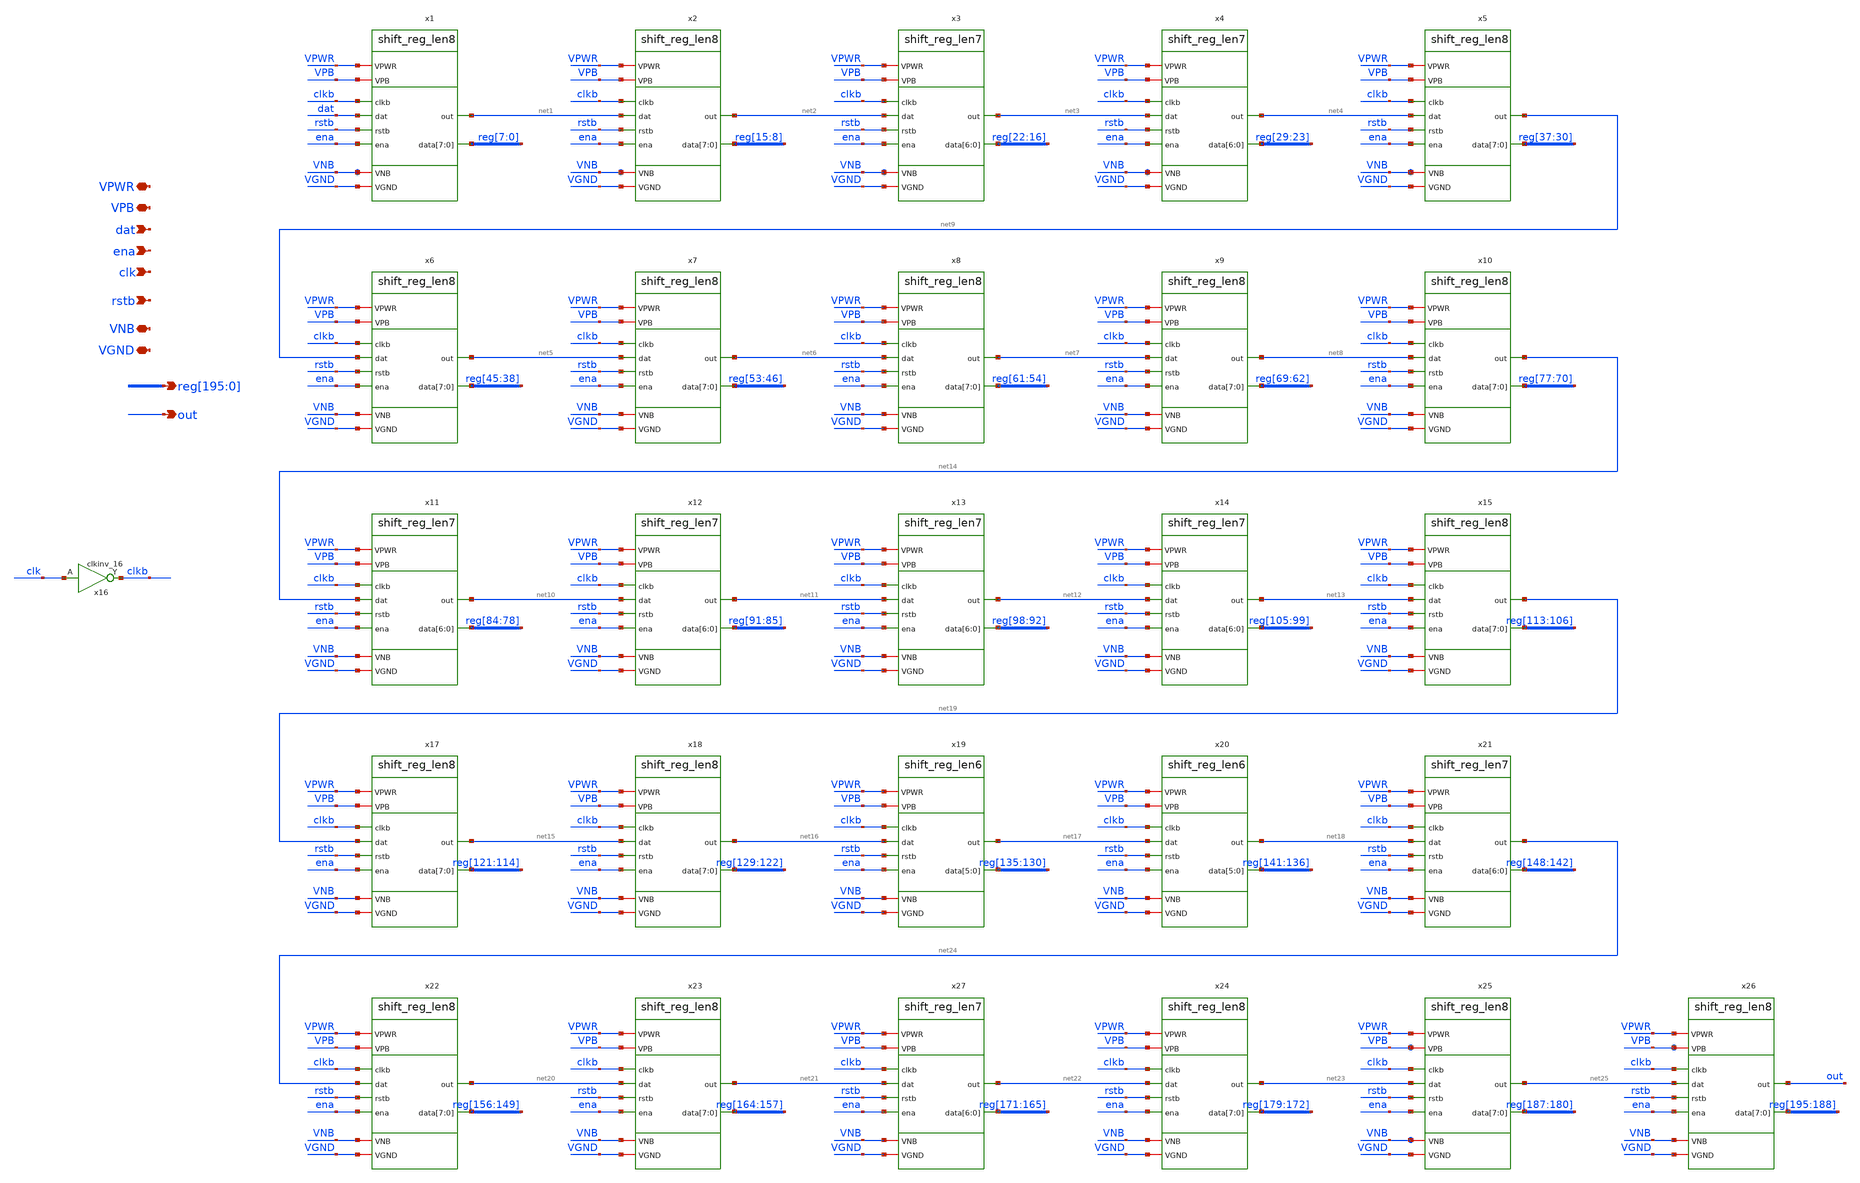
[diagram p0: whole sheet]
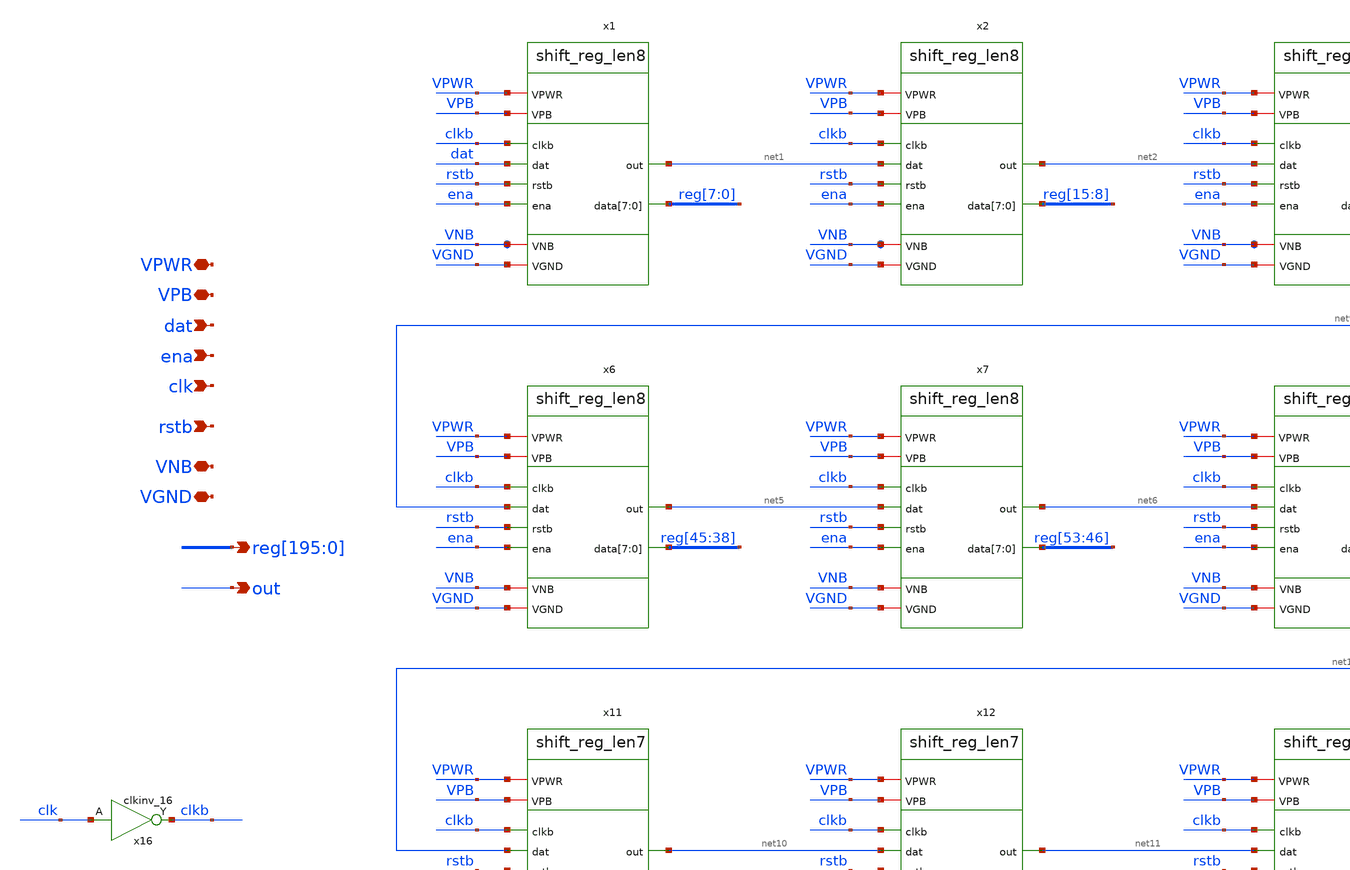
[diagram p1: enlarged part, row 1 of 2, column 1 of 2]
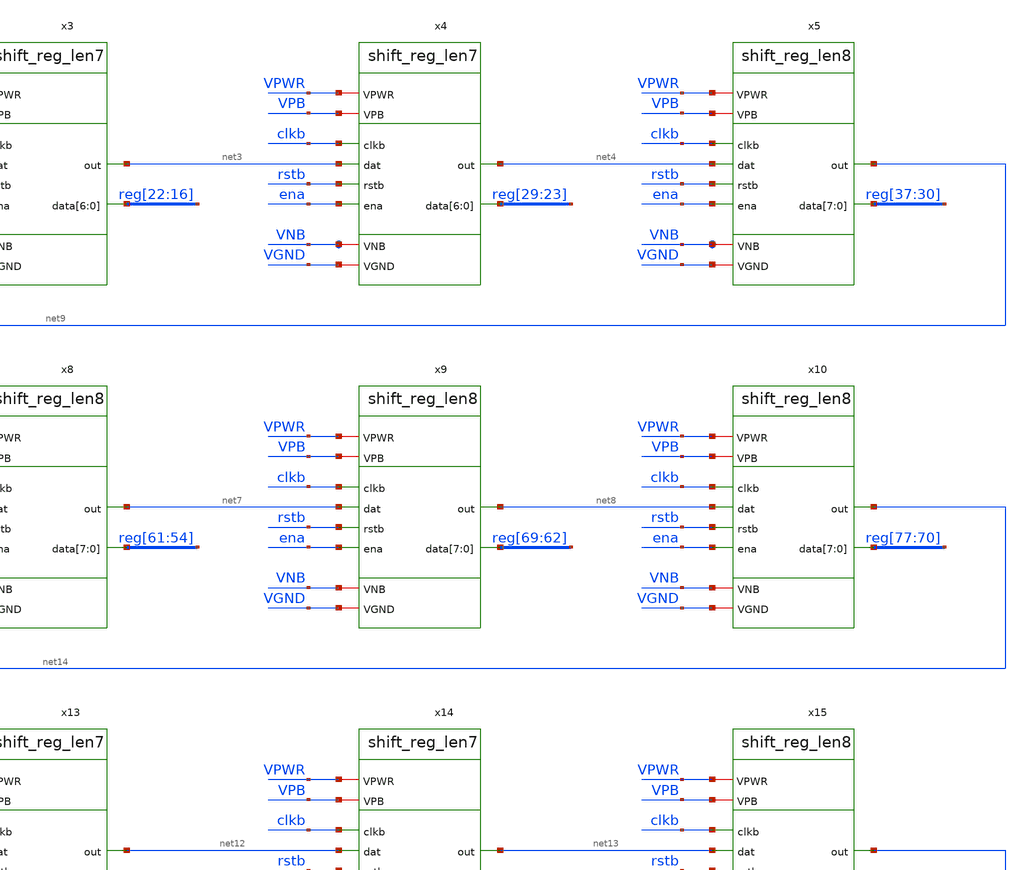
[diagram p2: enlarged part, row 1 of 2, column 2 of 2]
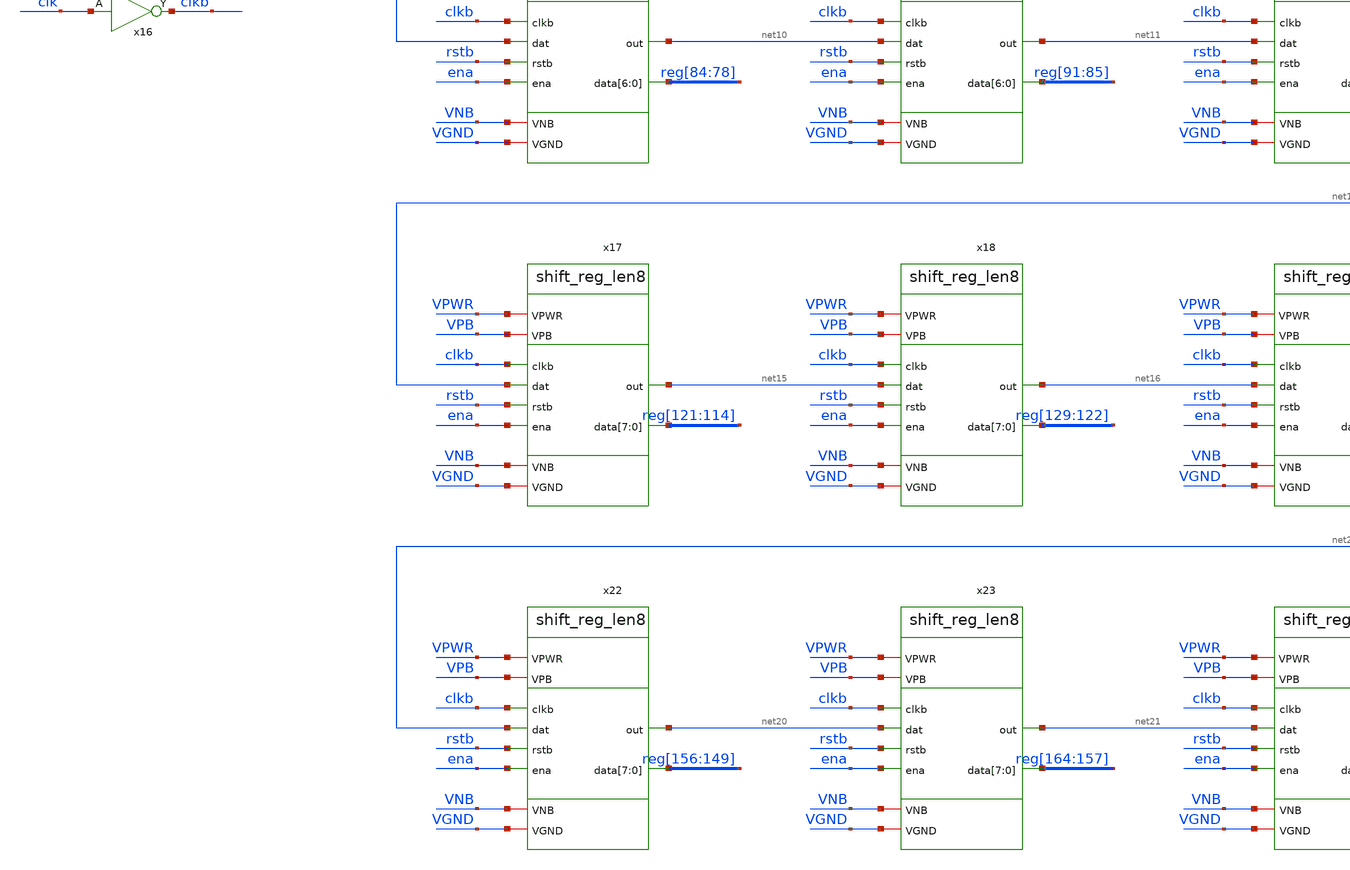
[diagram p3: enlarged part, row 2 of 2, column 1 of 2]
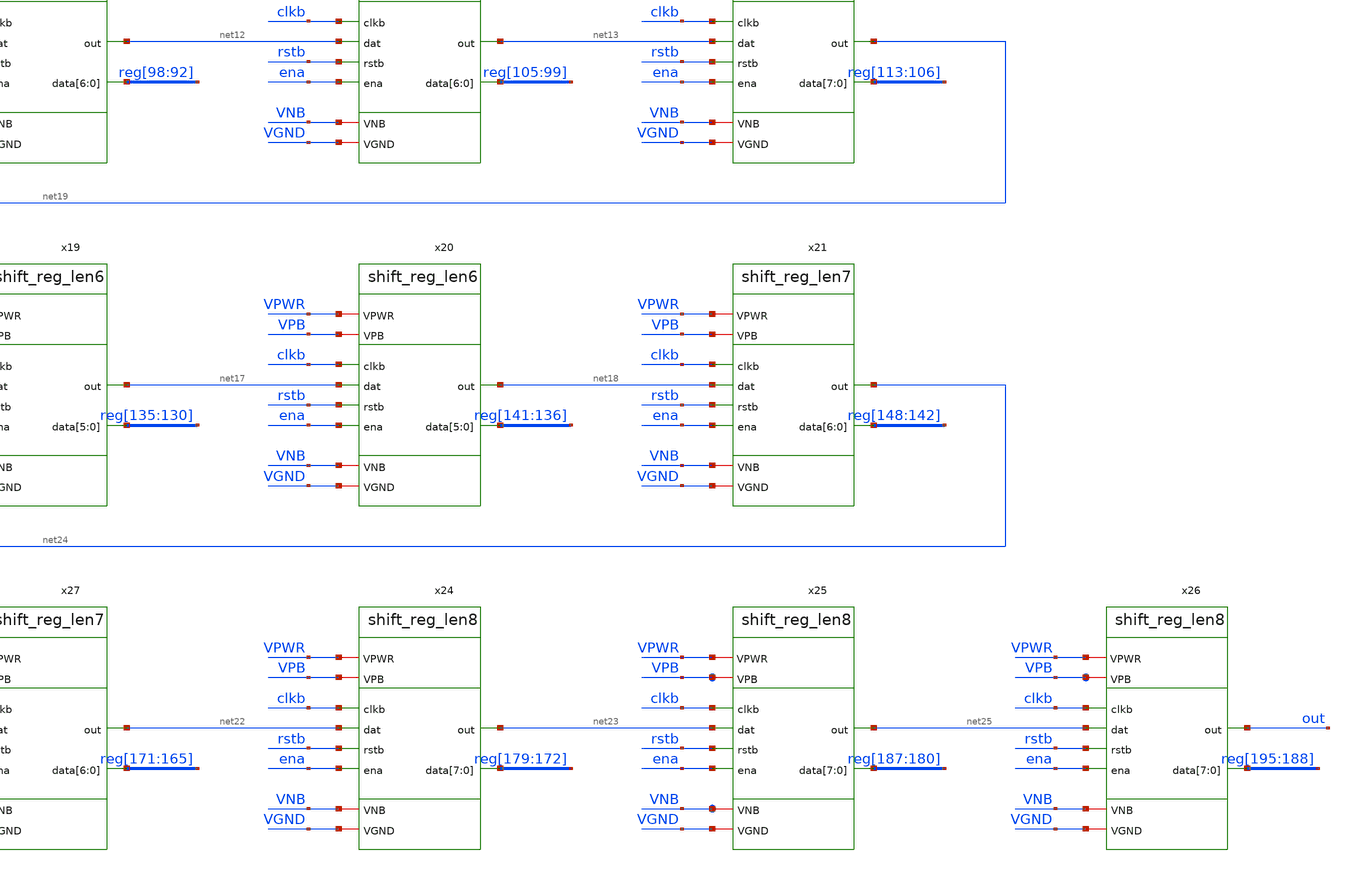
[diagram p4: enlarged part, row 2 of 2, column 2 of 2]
** sch_path: tt_um_mosbius/xschem/shift_reg.sch
**.subckt shift_reg clk dat rstb VPWR VGND
*+ reg[195],reg[194],reg[193],reg[192],reg[191],reg[190],reg[189],reg[188],reg[187],reg[186],reg[185],reg[184],reg[183],reg[182],reg[181],reg[180],reg[179],reg[178],reg[177],reg[176],reg[175],reg[174],reg[173],reg[172],reg[171],reg[170],reg[169],reg[168],reg[167],reg[166],reg[165],reg[164],reg[163],reg[162],reg[161],reg[160],reg[159],reg[158],reg[157],reg[156],reg[155],reg[154],reg[153],reg[152],reg[151],reg[150],reg[149],reg[148],reg[147],reg[146],reg[145],reg[144],reg[143],reg[142],reg[141],reg[140],reg[139],reg[138],reg[137],reg[136],reg[135],reg[134],reg[133],reg[132],reg[131],reg[130],reg[129],reg[128],reg[127],reg[126],reg[125],reg[124],reg[123],reg[122],reg[121],reg[120],reg[119],reg[118],reg[117],reg[116],reg[115],reg[114],reg[113],reg[112],reg[111],reg[110],reg[109],reg[108],reg[107],reg[106],reg[105],reg[104],reg[103],reg[102],reg[101],reg[100],reg[99],reg[98],reg[97],reg[96],reg[95],reg[94],reg[93],reg[92],reg[91],reg[90],reg[89],reg[88],reg[87],reg[86],reg[85],reg[84],reg[83],reg[82],reg[81],reg[80],reg[79],reg[78],reg[77],reg[76],reg[75],reg[74],reg[73],reg[72],reg[71],reg[70],reg[69],reg[68],reg[67],reg[66],reg[65],reg[64],reg[63],reg[62],reg[61],reg[60],reg[59],reg[58],reg[57],reg[56],reg[55],reg[54],reg[53],reg[52],reg[51],reg[50],reg[49],reg[48],reg[47],reg[46],reg[45],reg[44],reg[43],reg[42],reg[41],reg[40],reg[39],reg[38],reg[37],reg[36],reg[35],reg[34],reg[33],reg[32],reg[31],reg[30],reg[29],reg[28],reg[27],reg[26],reg[25],reg[24],reg[23],reg[22],reg[21],reg[20],reg[19],reg[18],reg[17],reg[16],reg[15],reg[14],reg[13],reg[12],reg[11],reg[10],reg[9],reg[8],reg[7],reg[6],reg[5],reg[4],reg[3],reg[2],reg[1],reg[0] ena out VPB VNB
*.ipin clk
*.ipin dat
*.ipin rstb
*.iopin VPWR
*.iopin VGND
*.opin
*+ reg[195],reg[194],reg[193],reg[192],reg[191],reg[190],reg[189],reg[188],reg[187],reg[186],reg[185],reg[184],reg[183],reg[182],reg[181],reg[180],reg[179],reg[178],reg[177],reg[176],reg[175],reg[174],reg[173],reg[172],reg[171],reg[170],reg[169],reg[168],reg[167],reg[166],reg[165],reg[164],reg[163],reg[162],reg[161],reg[160],reg[159],reg[158],reg[157],reg[156],reg[155],reg[154],reg[153],reg[152],reg[151],reg[150],reg[149],reg[148],reg[147],reg[146],reg[145],reg[144],reg[143],reg[142],reg[141],reg[140],reg[139],reg[138],reg[137],reg[136],reg[135],reg[134],reg[133],reg[132],reg[131],reg[130],reg[129],reg[128],reg[127],reg[126],reg[125],reg[124],reg[123],reg[122],reg[121],reg[120],reg[119],reg[118],reg[117],reg[116],reg[115],reg[114],reg[113],reg[112],reg[111],reg[110],reg[109],reg[108],reg[107],reg[106],reg[105],reg[104],reg[103],reg[102],reg[101],reg[100],reg[99],reg[98],reg[97],reg[96],reg[95],reg[94],reg[93],reg[92],reg[91],reg[90],reg[89],reg[88],reg[87],reg[86],reg[85],reg[84],reg[83],reg[82],reg[81],reg[80],reg[79],reg[78],reg[77],reg[76],reg[75],reg[74],reg[73],reg[72],reg[71],reg[70],reg[69],reg[68],reg[67],reg[66],reg[65],reg[64],reg[63],reg[62],reg[61],reg[60],reg[59],reg[58],reg[57],reg[56],reg[55],reg[54],reg[53],reg[52],reg[51],reg[50],reg[49],reg[48],reg[47],reg[46],reg[45],reg[44],reg[43],reg[42],reg[41],reg[40],reg[39],reg[38],reg[37],reg[36],reg[35],reg[34],reg[33],reg[32],reg[31],reg[30],reg[29],reg[28],reg[27],reg[26],reg[25],reg[24],reg[23],reg[22],reg[21],reg[20],reg[19],reg[18],reg[17],reg[16],reg[15],reg[14],reg[13],reg[12],reg[11],reg[10],reg[9],reg[8],reg[7],reg[6],reg[5],reg[4],reg[3],reg[2],reg[1],reg[0]
*.ipin ena
*.opin out
*.iopin VPB
*.iopin VNB
x1 VPWR net1 clkb dat rstb ena VGND reg[7] reg[6] reg[5] reg[4] reg[3] reg[2] reg[1] reg[0] VPB VNB
+ shift_reg_len8
x2 VPWR net2 clkb net1 rstb ena VGND reg[15] reg[14] reg[13] reg[12] reg[11] reg[10] reg[9] reg[8]
+ VPB VNB shift_reg_len8
x4 VPWR net4 clkb net3 rstb ena VGND reg[29] reg[28] reg[27] reg[26] reg[25] reg[24] reg[23] VPB VNB
+ shift_reg_len7
x5 VPWR net9 clkb net4 rstb ena VGND reg[37] reg[36] reg[35] reg[34] reg[33] reg[32] reg[31] reg[30]
+ VPB VNB shift_reg_len8
x6 VPWR net5 clkb net9 rstb ena VGND reg[45] reg[44] reg[43] reg[42] reg[41] reg[40] reg[39] reg[38]
+ VPB VNB shift_reg_len8
x7 VPWR net6 clkb net5 rstb ena VGND reg[53] reg[52] reg[51] reg[50] reg[49] reg[48] reg[47] reg[46]
+ VPB VNB shift_reg_len8
x8 VPWR net7 clkb net6 rstb ena VGND reg[61] reg[60] reg[59] reg[58] reg[57] reg[56] reg[55] reg[54]
+ VPB VNB shift_reg_len8
x9 VPWR net8 clkb net7 rstb ena VGND reg[69] reg[68] reg[67] reg[66] reg[65] reg[64] reg[63] reg[62]
+ VPB VNB shift_reg_len8
x10 VPWR net14 clkb net8 rstb ena VGND reg[77] reg[76] reg[75] reg[74] reg[73] reg[72] reg[71]
+ reg[70] VPB VNB shift_reg_len8
x15 VPWR net19 clkb net13 rstb ena VGND reg[113] reg[112] reg[111] reg[110] reg[109] reg[108]
+ reg[107] reg[106] VPB VNB shift_reg_len8
x11 VPWR net10 clkb net14 rstb ena VGND reg[84] reg[83] reg[82] reg[81] reg[80] reg[79] reg[78] VPB
+ VNB shift_reg_len7
x12 VPWR net11 clkb net10 rstb ena VGND reg[91] reg[90] reg[89] reg[88] reg[87] reg[86] reg[85] VPB
+ VNB shift_reg_len7
x13 VPWR net12 clkb net11 rstb ena VGND reg[98] reg[97] reg[96] reg[95] reg[94] reg[93] reg[92] VPB
+ VNB shift_reg_len7
x14 VPWR net13 clkb net12 rstb ena VGND reg[105] reg[104] reg[103] reg[102] reg[101] reg[100]
+ reg[99] VPB VNB shift_reg_len7
x3 VPWR net3 clkb net2 rstb ena VGND reg[22] reg[21] reg[20] reg[19] reg[18] reg[17] reg[16] VPB VNB
+ shift_reg_len7
x17 VPWR net15 clkb net19 rstb ena VGND reg[121] reg[120] reg[119] reg[118] reg[117] reg[116]
+ reg[115] reg[114] VPB VNB shift_reg_len8
x18 VPWR net16 clkb net15 rstb ena VGND reg[129] reg[128] reg[127] reg[126] reg[125] reg[124]
+ reg[123] reg[122] VPB VNB shift_reg_len8
x19 VPWR net17 clkb net16 rstb ena VGND reg[135] reg[134] reg[133] reg[132] reg[131] reg[130] VPB
+ VNB shift_reg_len6
x20 VPWR net18 clkb net17 rstb ena VGND reg[141] reg[140] reg[139] reg[138] reg[137] reg[136] VPB
+ VNB shift_reg_len6
x21 VPWR net24 clkb net18 rstb ena VGND reg[148] reg[147] reg[146] reg[145] reg[144] reg[143]
+ reg[142] VPB VNB shift_reg_len7
x22 VPWR net20 clkb net24 rstb ena VGND reg[156] reg[155] reg[154] reg[153] reg[152] reg[151]
+ reg[150] reg[149] VPB VNB shift_reg_len8
x23 VPWR net21 clkb net20 rstb ena VGND reg[164] reg[163] reg[162] reg[161] reg[160] reg[159]
+ reg[158] reg[157] VPB VNB shift_reg_len8
x24 VPWR net23 clkb net22 rstb ena VGND reg[179] reg[178] reg[177] reg[176] reg[175] reg[174]
+ reg[173] reg[172] VPB VNB shift_reg_len8
x25 VPWR net25 clkb net23 rstb ena VGND reg[187] reg[186] reg[185] reg[184] reg[183] reg[182]
+ reg[181] reg[180] VPB VNB shift_reg_len8
x26 VPWR out clkb net25 rstb ena VGND reg[195] reg[194] reg[193] reg[192] reg[191] reg[190] reg[189]
+ reg[188] VPB VNB shift_reg_len8
x27 VPWR net22 clkb net21 rstb ena VGND reg[171] reg[170] reg[169] reg[168] reg[167] reg[166]
+ reg[165] VPB VNB shift_reg_len7
x16 clk VGND VNB VPB VPWR clkb sky130_fd_sc_hd__clkinv_16
**.ends

* expanding   symbol:  shift_reg_len8.sym # of pins=10
** sym_path: tt_um_mosbius/xschem/shift_reg_len8.sym
** sch_path: tt_um_mosbius/xschem/shift_reg_len8.sch
.subckt shift_reg_len8 VPWR out clkb dat rstb ena VGND data[7] data[6] data[5] data[4] data[3]
+ data[2] data[1] data[0] VPB VNB
*.ipin clkb
*.ipin dat
*.ipin rstb
*.iopin VPWR
*.opin data[7],data[6],data[5],data[4],data[3],data[2],data[1],data[0]
*.ipin ena
*.opin out
*.iopin VGND
*.iopin VPB
*.iopin VNB
x10[7] out ena VGND VNB VPB VPWR data[7] sky130_fd_sc_hd__and2_1
x10[6] reg[6] ena VGND VNB VPB VPWR data[6] sky130_fd_sc_hd__and2_1
x10[5] reg[5] ena VGND VNB VPB VPWR data[5] sky130_fd_sc_hd__and2_1
x10[4] reg[4] ena VGND VNB VPB VPWR data[4] sky130_fd_sc_hd__and2_1
x10[3] reg[3] ena VGND VNB VPB VPWR data[3] sky130_fd_sc_hd__and2_1
x10[2] reg[2] ena VGND VNB VPB VPWR data[2] sky130_fd_sc_hd__and2_1
x10[1] reg[1] ena VGND VNB VPB VPWR data[1] sky130_fd_sc_hd__and2_1
x10[0] reg[0] ena VGND VNB VPB VPWR data[0] sky130_fd_sc_hd__and2_1
x1 clk dat rstb VGND VNB VPB VPWR reg[0] sky130_fd_sc_hd__dfrtp_1
x2 clk reg[0] rstb VGND VNB VPB VPWR reg[1] sky130_fd_sc_hd__dfrtp_1
x3 clk reg[1] rstb VGND VNB VPB VPWR reg[2] sky130_fd_sc_hd__dfrtp_1
x4 clk reg[2] rstb VGND VNB VPB VPWR reg[3] sky130_fd_sc_hd__dfrtp_1
x5 clk reg[3] rstb VGND VNB VPB VPWR reg[4] sky130_fd_sc_hd__dfrtp_1
x6 clk reg[4] rstb VGND VNB VPB VPWR reg[5] sky130_fd_sc_hd__dfrtp_1
x7 clk reg[5] rstb VGND VNB VPB VPWR reg[6] sky130_fd_sc_hd__dfrtp_1
x8 clk reg[6] rstb VGND VNB VPB VPWR out sky130_fd_sc_hd__dfrtp_1
x9 clkb VGND VNB VPB VPWR clk sky130_fd_sc_hd__clkinv_1
.ends


* expanding   symbol:  shift_reg_len7.sym # of pins=10
** sym_path: tt_um_mosbius/xschem/shift_reg_len7.sym
** sch_path: tt_um_mosbius/xschem/shift_reg_len7.sch
.subckt shift_reg_len7 VPWR out clkb dat rstb ena VGND data[6] data[5] data[4] data[3] data[2]
+ data[1] data[0] VPB VNB
*.ipin clkb
*.ipin dat
*.ipin rstb
*.iopin VPWR
*.iopin VGND
*.opin data[6],data[5],data[4],data[3],data[2],data[1],data[0]
*.ipin ena
*.opin out
*.iopin VPB
*.iopin VNB
x8 clkb VGND VNB VPB VPWR clk sky130_fd_sc_hd__clkinv_1
x9[6] out ena VGND VNB VPB VPWR data[6] sky130_fd_sc_hd__and2_1
x9[5] reg[5] ena VGND VNB VPB VPWR data[5] sky130_fd_sc_hd__and2_1
x9[4] reg[4] ena VGND VNB VPB VPWR data[4] sky130_fd_sc_hd__and2_1
x9[3] reg[3] ena VGND VNB VPB VPWR data[3] sky130_fd_sc_hd__and2_1
x9[2] reg[2] ena VGND VNB VPB VPWR data[2] sky130_fd_sc_hd__and2_1
x9[1] reg[1] ena VGND VNB VPB VPWR data[1] sky130_fd_sc_hd__and2_1
x9[0] reg[0] ena VGND VNB VPB VPWR data[0] sky130_fd_sc_hd__and2_1
x1 clk dat rstb VGND VNB VPB VPWR reg[0] sky130_fd_sc_hd__dfrtp_1
x2 clk reg[0] rstb VGND VNB VPB VPWR reg[1] sky130_fd_sc_hd__dfrtp_1
x3 clk reg[1] rstb VGND VNB VPB VPWR reg[2] sky130_fd_sc_hd__dfrtp_1
x4 clk reg[2] rstb VGND VNB VPB VPWR reg[3] sky130_fd_sc_hd__dfrtp_1
x5 clk reg[3] rstb VGND VNB VPB VPWR reg[4] sky130_fd_sc_hd__dfrtp_1
x6 clk reg[4] rstb VGND VNB VPB VPWR reg[5] sky130_fd_sc_hd__dfrtp_1
x7 clk reg[5] rstb VGND VNB VPB VPWR out sky130_fd_sc_hd__dfrtp_1
.ends


* expanding   symbol:  shift_reg_len6.sym # of pins=10
** sym_path: tt_um_mosbius/xschem/shift_reg_len6.sym
** sch_path: tt_um_mosbius/xschem/shift_reg_len6.sch
.subckt shift_reg_len6 VPWR out clkb dat rstb ena VGND data[5] data[4] data[3] data[2] data[1]
+ data[0] VPB VNB
*.ipin clkb
*.ipin dat
*.ipin rstb
*.iopin VPWR
*.iopin VGND
*.opin data[5],data[4],data[3],data[2],data[1],data[0]
*.ipin ena
*.opin out
*.iopin VPB
*.iopin VNB
x7 clkb VGND VNB VPB VPWR clk sky130_fd_sc_hd__clkinv_1
x8[5] out ena VGND VNB VPB VPWR data[5] sky130_fd_sc_hd__and2_1
x8[4] reg[4] ena VGND VNB VPB VPWR data[4] sky130_fd_sc_hd__and2_1
x8[3] reg[3] ena VGND VNB VPB VPWR data[3] sky130_fd_sc_hd__and2_1
x8[2] reg[2] ena VGND VNB VPB VPWR data[2] sky130_fd_sc_hd__and2_1
x8[1] reg[1] ena VGND VNB VPB VPWR data[1] sky130_fd_sc_hd__and2_1
x8[0] reg[0] ena VGND VNB VPB VPWR data[0] sky130_fd_sc_hd__and2_1
x8 clk dat rstb VGND VNB VPB VPWR reg[0] sky130_fd_sc_hd__dfrtp_1
x1 clk reg[0] rstb VGND VNB VPB VPWR reg[1] sky130_fd_sc_hd__dfrtp_1
x2 clk reg[1] rstb VGND VNB VPB VPWR reg[2] sky130_fd_sc_hd__dfrtp_1
x3 clk reg[2] rstb VGND VNB VPB VPWR reg[3] sky130_fd_sc_hd__dfrtp_1
x4 clk reg[3] rstb VGND VNB VPB VPWR reg[4] sky130_fd_sc_hd__dfrtp_1
x5 clk reg[4] rstb VGND VNB VPB VPWR out sky130_fd_sc_hd__dfrtp_1
.ends

.end
